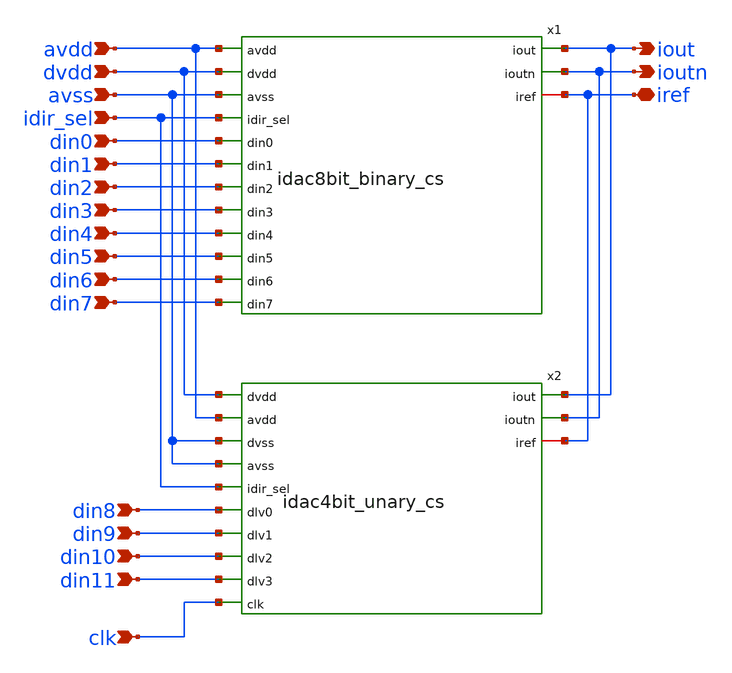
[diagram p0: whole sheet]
** sch_path: xschem/idac12bitsegmented.sch
**.subckt idac12bitsegmented avdd dvdd avss idir_sel din0 din1 din2 din3 din4 din5 din7 din8 din9
*+ din10 din6 din11 iout ioutn iref clk
*.ipin avdd
*.ipin dvdd
*.ipin avss
*.ipin idir_sel
*.ipin din0
*.ipin din1
*.ipin din2
*.ipin din3
*.ipin din4
*.ipin din5
*.ipin din7
*.ipin din8
*.ipin din9
*.ipin din10
*.ipin din6
*.ipin din11
*.opin iout
*.opin ioutn
*.iopin iref
*.ipin clk
x1 avdd dvdd iout ioutn din0 idir_sel din1 avss din2 din3 iref din4 din5 din6 din7
+ idac8bit_binary_cs
x2 dvdd iout avdd ioutn avss avss idir_sel din8 din9 din10 din11 clk iref idac4bit_unary_cs
**.ends
.end
